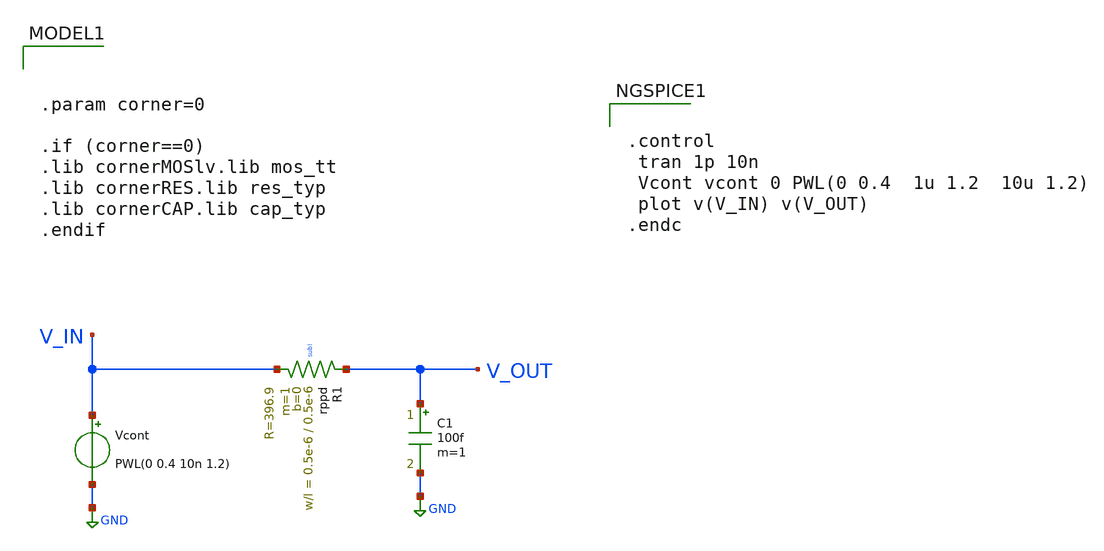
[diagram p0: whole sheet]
** sch_path: others/voltage_ramp.sch
**.subckt voltage_ramp
Vcont V_IN GND PWL(0 0.4 10n 1.2)
C1 V_OUT GND 100f m=1
XR1 V_OUT V_IN sub! rppd w=0.5e-6 l=0.5e-6 m=1 b=0 mm_ok=1
**** begin user architecture code


.param corner=0

.if (corner==0)
.lib cornerMOSlv.lib mos_tt
.lib cornerRES.lib res_typ
.lib cornerCAP.lib cap_typ
.endif



.control
 tran 1p 10n
 Vcont vcont 0 PWL(0 0.4  1u 1.2  10u 1.2)
 plot v(V_IN) v(V_OUT)
.endc


**** end user architecture code
**.ends
.GLOBAL GND
.end
